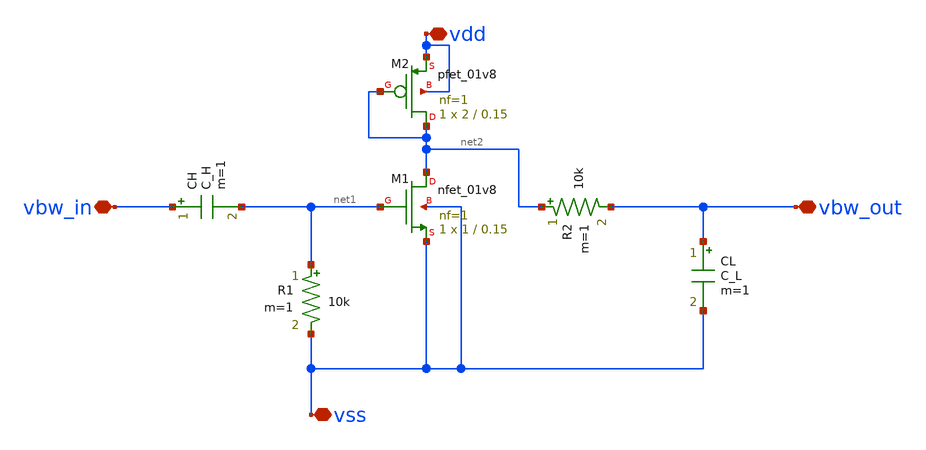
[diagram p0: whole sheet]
** sch_path: Synapse/bpfilter.sch
**.subckt bpfilter vbw_in vbw_out vss vdd
*.iopin vbw_in
*.iopin vbw_out
*.iopin vss
*.iopin vdd
R1 net1 vss 10k m=1
R2 net2 vbw_out 10k m=1
CL vbw_out vss C_L m=1
CH vbw_in net1 C_H m=1
XM1 net2 net1 vss vss sky130_fd_pr__nfet_01v8 L=0.15 W=1 nf=1 ad='int((nf+1)/2) * W/nf * 0.29' as='int((nf+2)/2) * W/nf * 0.29'
+ pd='2*int((nf+1)/2) * (W/nf + 0.29)' ps='2*int((nf+2)/2) * (W/nf + 0.29)' nrd='0.29 / W' nrs='0.29 / W'
+ sa=0 sb=0 sd=0 mult=1 m=1
XM2 net2 net2 vdd vdd sky130_fd_pr__pfet_01v8 L=0.15 W=2 nf=1 ad='int((nf+1)/2) * W/nf * 0.29' as='int((nf+2)/2) * W/nf * 0.29'
+ pd='2*int((nf+1)/2) * (W/nf + 0.29)' ps='2*int((nf+2)/2) * (W/nf + 0.29)' nrd='0.29 / W' nrs='0.29 / W'
+ sa=0 sb=0 sd=0 mult=1 m=1
**.ends
.end
